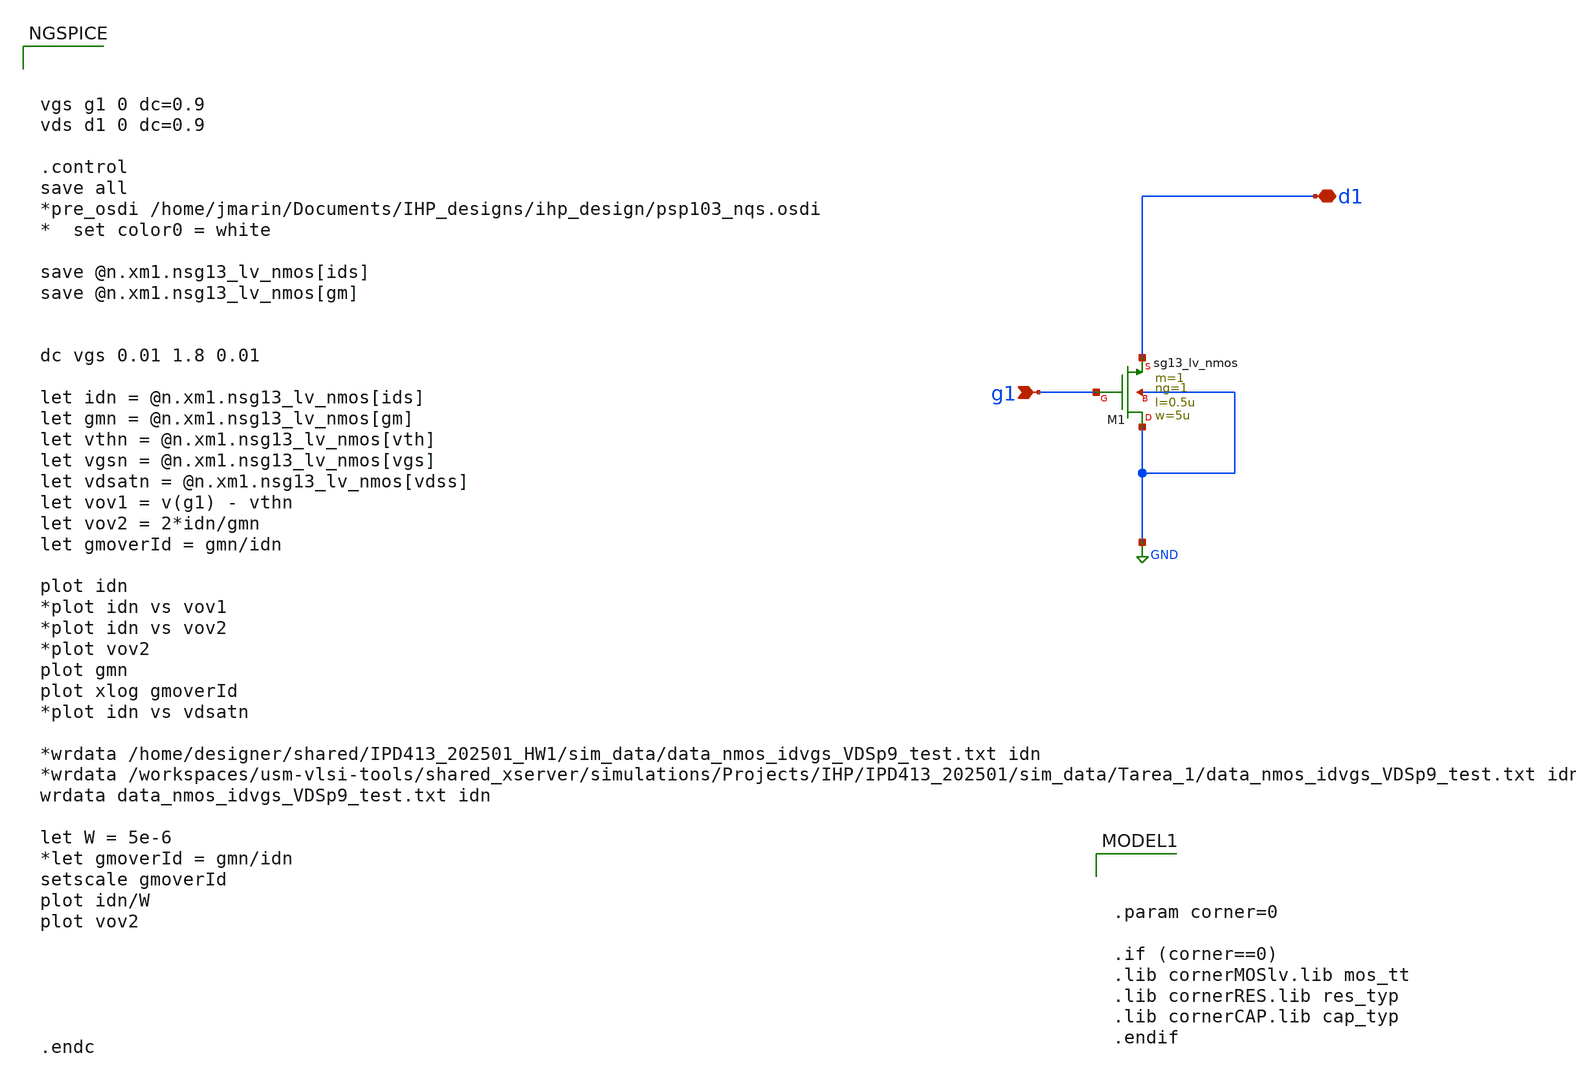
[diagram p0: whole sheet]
** sch_path: xschem/Tareas/Tarea_1/nmoslv_charac_IPD413-202501-HW1.sch
**.subckt nmoslv_charac_IPD413-202501-HW1 g1 d1
*.ipin g1
*.iopin d1
XM1 GND g1 d1 GND sg13_lv_nmos w=5u l=0.5u ng=1 m=1 mm_ok=1
**** begin user architecture code



vgs g1 0 dc=0.9
vds d1 0 dc=0.9

.control
save all
*pre_osdi /home/jmarin/Documents/IHP_designs/ihp_design/psp103_nqs.osdi
*  set color0 = white

save @n.xm1.nsg13_lv_nmos[ids]
save @n.xm1.nsg13_lv_nmos[gm]


dc vgs 0.01 1.8 0.01

let idn = @n.xm1.nsg13_lv_nmos[ids]
let gmn = @n.xm1.nsg13_lv_nmos[gm]
let vthn = @n.xm1.nsg13_lv_nmos[vth]
let vgsn = @n.xm1.nsg13_lv_nmos[vgs]
let vdsatn = @n.xm1.nsg13_lv_nmos[vdss]
let vov1 = v(g1) - vthn
let vov2 = 2*idn/gmn
let gmoverId = gmn/idn

plot idn
*plot idn vs vov1
*plot idn vs vov2
*plot vov2
plot gmn
plot xlog gmoverId
*plot idn vs vdsatn

*wrdata /home/designer/shared/IPD413_202501_HW1/sim_data/data_nmos_idvgs_VDSp9_test.txt idn
*wrdata
*+ /workspaces/usm-vlsi-tools/shared_xserver/simulations/Projects/IHP/IPD413_202501/sim_data/Tarea_1/data_nmos_idvgs_VDSp9_test.txt idn
wrdata data_nmos_idvgs_VDSp9_test.txt idn

let W = 5e-6
*let gmoverId = gmn/idn
setscale gmoverId
plot idn/W
plot vov2





.endc




.param corner=0

.if (corner==0)
.lib cornerMOSlv.lib mos_tt
.lib cornerRES.lib res_typ
.lib cornerCAP.lib cap_typ
.endif

**** end user architecture code
**.ends
.GLOBAL GND
.end
